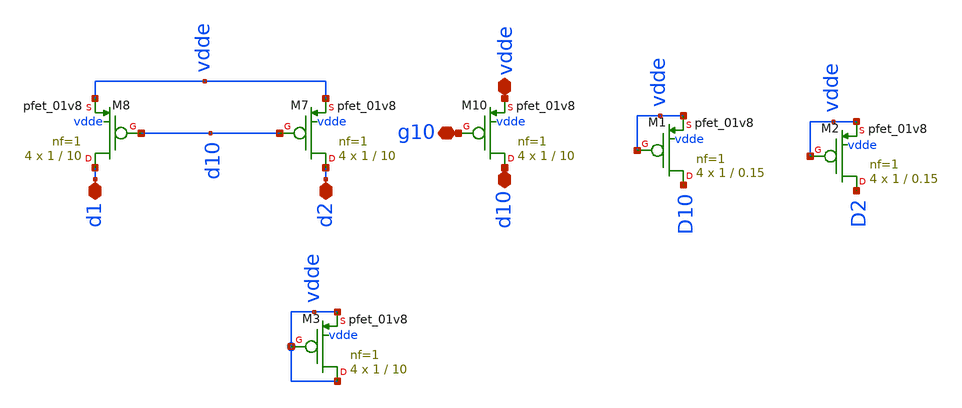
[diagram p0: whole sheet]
** sch_path: magic/pmos_current_bgr.sch
**.subckt pmos_current_bgr vdde g10 d10 d2 d1
*.iopin vdde
*.iopin g10
*.iopin d10
*.iopin d2
*.iopin d1
XM10 d10 g10 vdde vdde sky130_fd_pr__pfet_01v8 L=10 W=1 nf=1 ad='int((nf+1)/2) * W/nf * 0.29' as='int((nf+2)/2) * W/nf * 0.29'
+ pd='2*int((nf+1)/2) * (W/nf + 0.29)' ps='2*int((nf+2)/2) * (W/nf + 0.29)' nrd='0.29 / W' nrs='0.29 / W'
+ sa=0 sb=0 sd=0 mult=4 m=4
XM7 d2 d10 vdde vdde sky130_fd_pr__pfet_01v8 L=10 W=1 nf=1 ad='int((nf+1)/2) * W/nf * 0.29' as='int((nf+2)/2) * W/nf * 0.29'
+ pd='2*int((nf+1)/2) * (W/nf + 0.29)' ps='2*int((nf+2)/2) * (W/nf + 0.29)' nrd='0.29 / W' nrs='0.29 / W'
+ sa=0 sb=0 sd=0 mult=4 m=4
XM8 d1 d10 vdde vdde sky130_fd_pr__pfet_01v8 L=10 W=1 nf=1 ad='int((nf+1)/2) * W/nf * 0.29' as='int((nf+2)/2) * W/nf * 0.29'
+ pd='2*int((nf+1)/2) * (W/nf + 0.29)' ps='2*int((nf+2)/2) * (W/nf + 0.29)' nrd='0.29 / W' nrs='0.29 / W'
+ sa=0 sb=0 sd=0 mult=4 m=4
XM1 D10 vdde vdde vdde sky130_fd_pr__pfet_01v8 L=0.15 W=1 nf=1 ad='int((nf+1)/2) * W/nf * 0.29' as='int((nf+2)/2) * W/nf * 0.29'
+ pd='2*int((nf+1)/2) * (W/nf + 0.29)' ps='2*int((nf+2)/2) * (W/nf + 0.29)' nrd='0.29 / W' nrs='0.29 / W'
+ sa=0 sb=0 sd=0 mult=4 m=4
XM2 D2 vdde vdde vdde sky130_fd_pr__pfet_01v8 L=0.15 W=1 nf=1 ad='int((nf+1)/2) * W/nf * 0.29' as='int((nf+2)/2) * W/nf * 0.29'
+ pd='2*int((nf+1)/2) * (W/nf + 0.29)' ps='2*int((nf+2)/2) * (W/nf + 0.29)' nrd='0.29 / W' nrs='0.29 / W'
+ sa=0 sb=0 sd=0 mult=4 m=4
XM3 vdde vdde vdde vdde sky130_fd_pr__pfet_01v8 L=10 W=1 nf=1 ad='int((nf+1)/2) * W/nf * 0.29' as='int((nf+2)/2) * W/nf * 0.29'
+ pd='2*int((nf+1)/2) * (W/nf + 0.29)' ps='2*int((nf+2)/2) * (W/nf + 0.29)' nrd='0.29 / W' nrs='0.29 / W'
+ sa=0 sb=0 sd=0 mult=4 m=4
**.ends
.end
